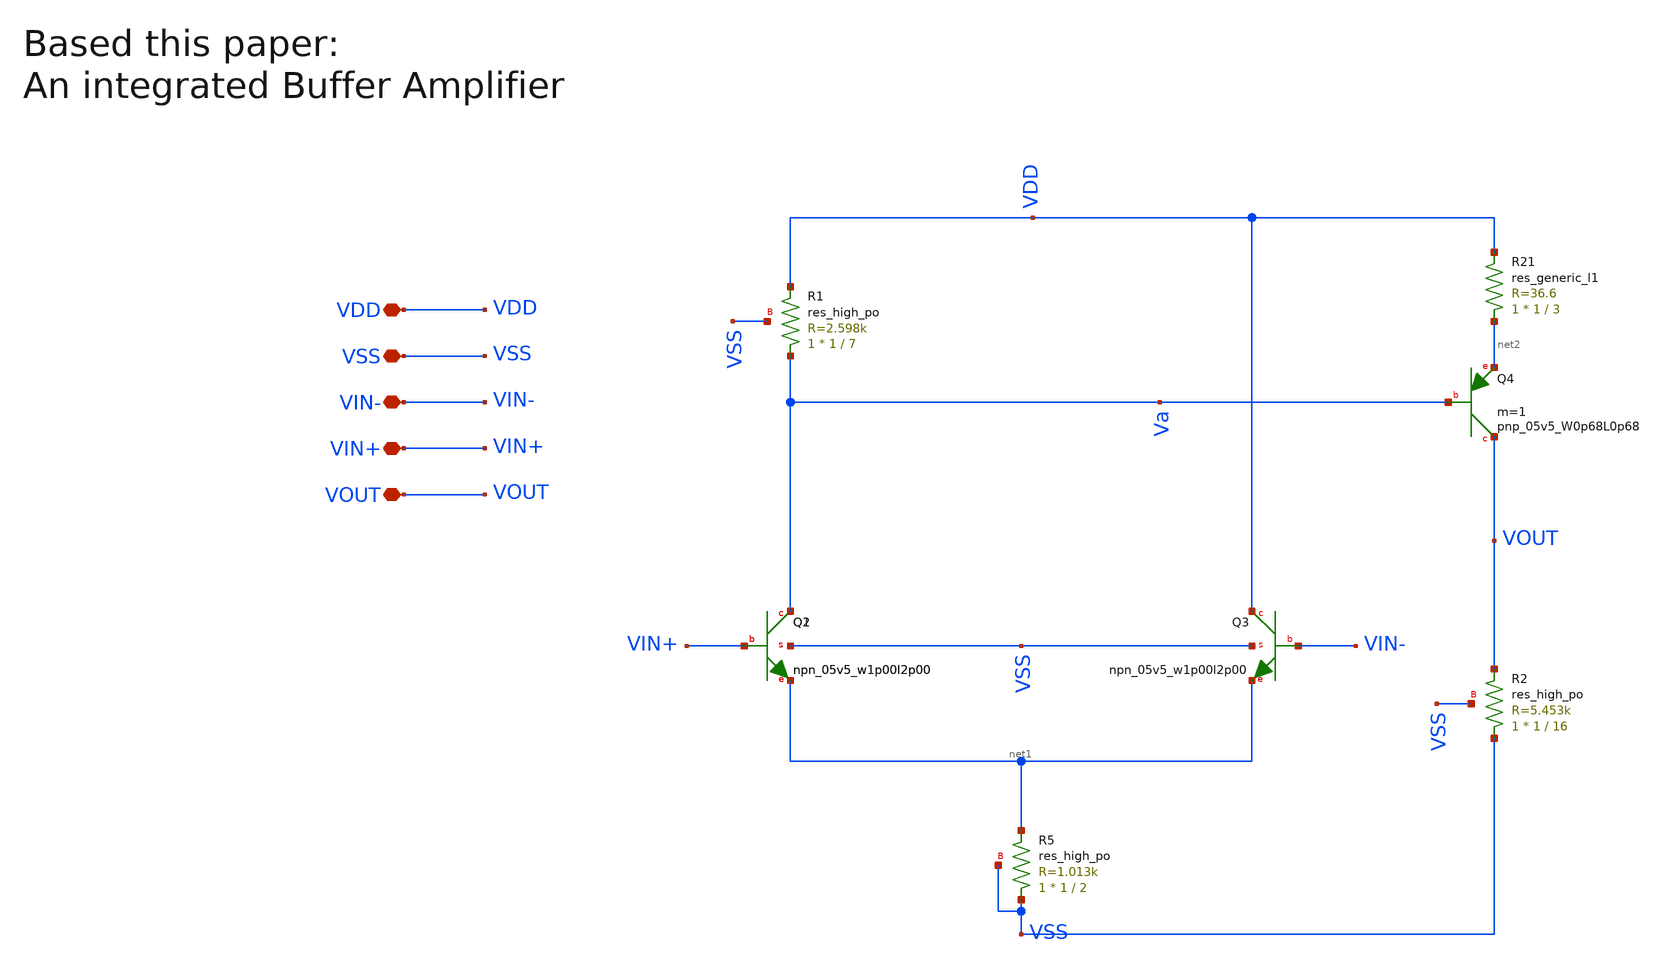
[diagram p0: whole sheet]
** sch_path: my_ip/LIB/Sky130A/single ended amplifiers/BIP001_PMOS_5_sky130A.sch
**.subckt BIP001_PMOS_5_sky130A VDD VSS VIN- VIN+ VOUT
*.iopin VDD
*.iopin VSS
*.iopin VIN-
*.iopin VIN+
*.iopin VOUT
XQ2 Va VIN+ net1 VSS sky130_fd_pr__npn_05v5_w1p00l2p00
XQ1 Va VIN+ net1 VSS sky130_fd_pr__npn_05v5_w1p00l2p00
XQ3 VDD VIN- net1 VSS sky130_fd_pr__npn_05v5_w1p00l2p00
XR5 VSS net1 VSS sky130_fd_pr__res_high_po W=1 L=2 mult=1 m=1
XR1 Va VDD VSS sky130_fd_pr__res_high_po W=1 L=7 mult=1 m=1
XQ4 VOUT Va net2 sky130_fd_pr__pnp_05v5_W0p68L0p68 m=1
R21 net2 VDD sky130_fd_pr__res_generic_l1 W=1 L=3 m=1
XR2 VSS VOUT VSS sky130_fd_pr__res_high_po W=1 L=16 mult=1 m=1
**.ends
.end
